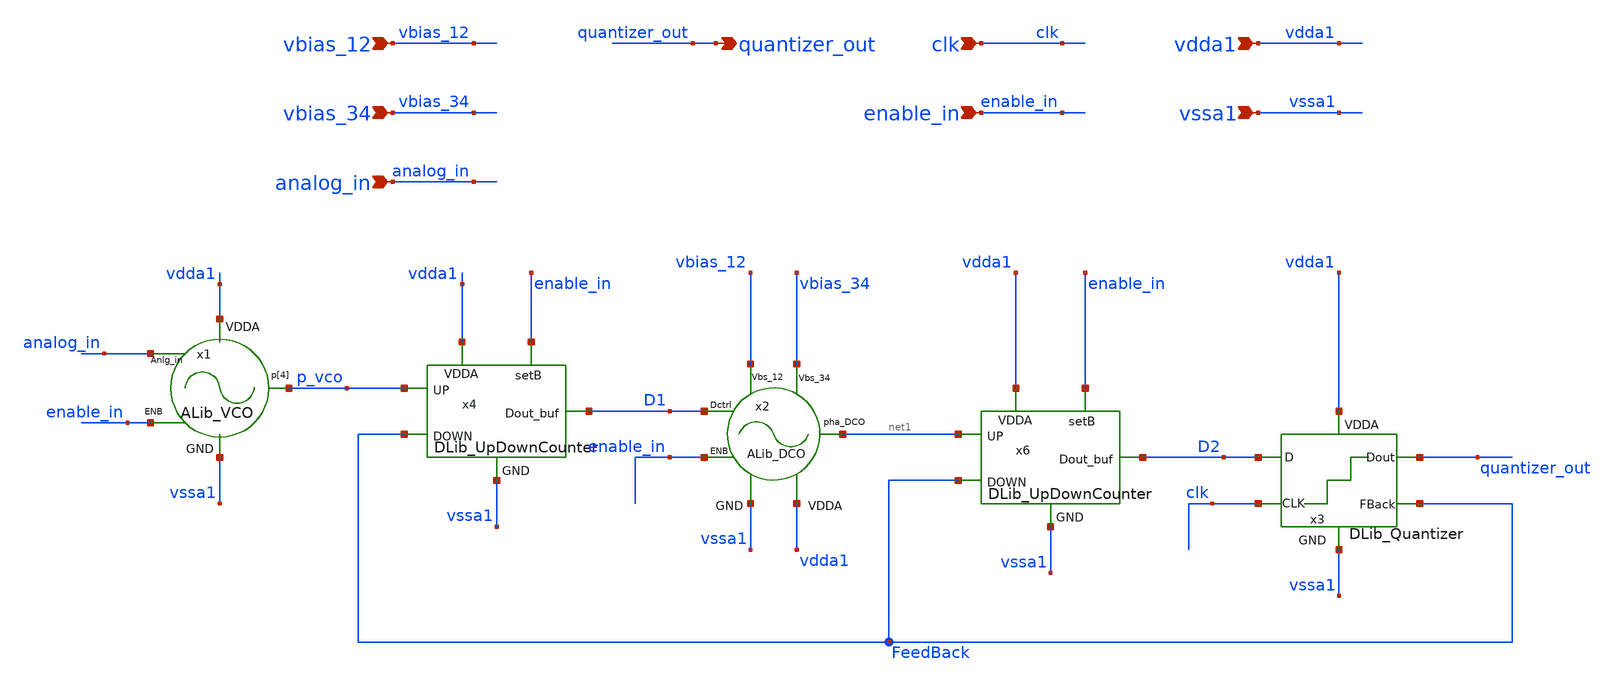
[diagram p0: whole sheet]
** sch_path: xschem/lib/vco_adc2.sch
**.subckt vco_adc2 vdda1 quantizer_out vssa1 enable_in clk vbias_34 analog_in vbias_12
*.ipin vdda1
*.opin quantizer_out
*.ipin vssa1
*.ipin enable_in
*.ipin clk
*.ipin vbias_34
*.ipin analog_in
*.ipin vbias_12
x1 analog_in enable_in p_vco vdda1 vssa1 ALib_VCO
x2 vbias_12 vbias_34 net1 D1 enable_in vdda1 vssa1 ALib_DCO
x3 vdda1 vssa1 clk quantizer_out FeedBack D2 DLib_Quantizer
x4 vdda1 vssa1 p_vco enable_in FeedBack D1 DLib_UpDownCounter
x6 vdda1 vssa1 net1 enable_in FeedBack D2 DLib_UpDownCounter
**.ends
.end
